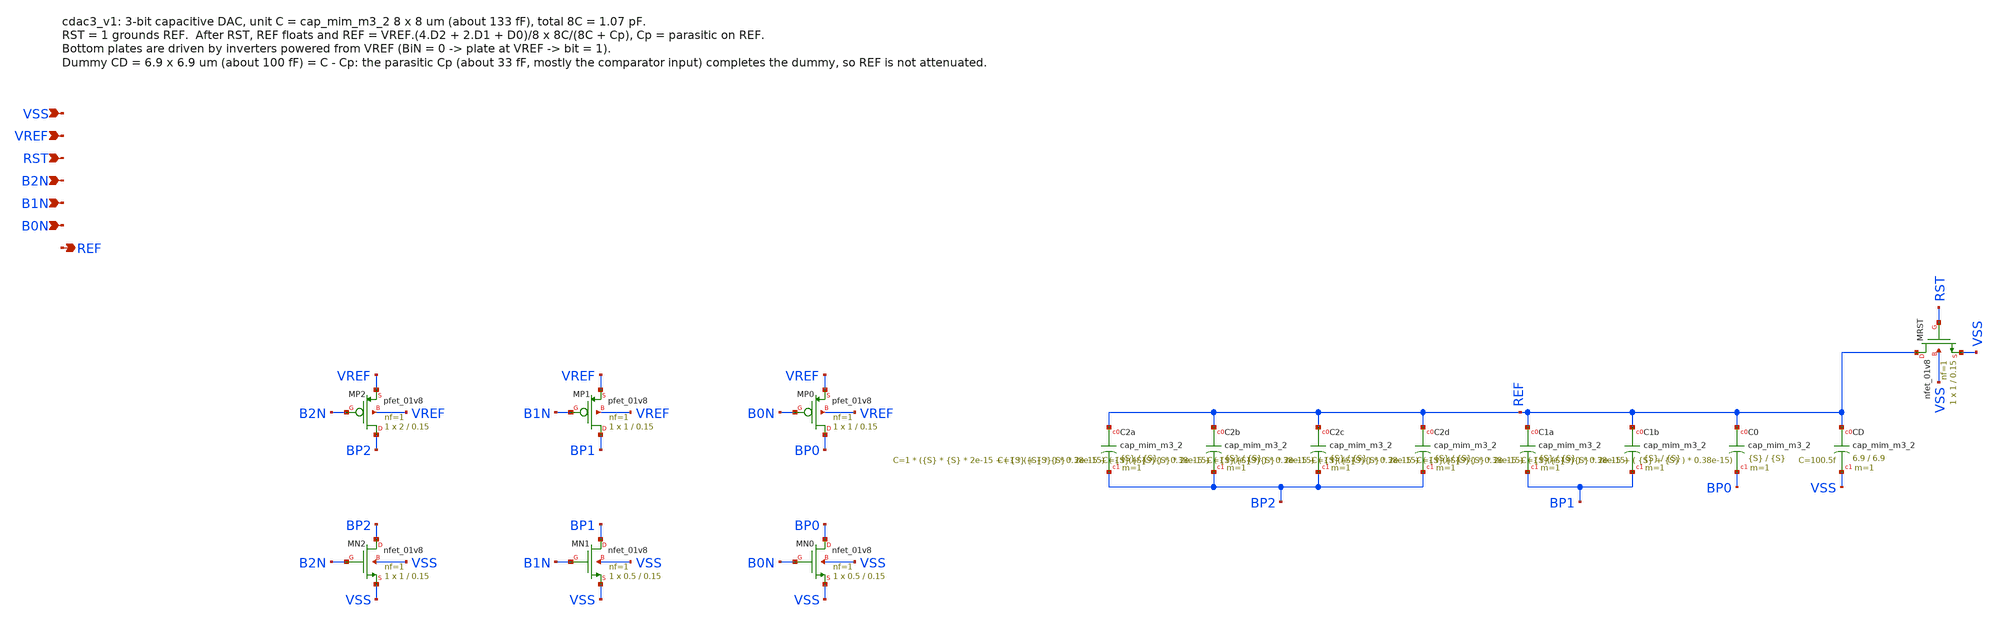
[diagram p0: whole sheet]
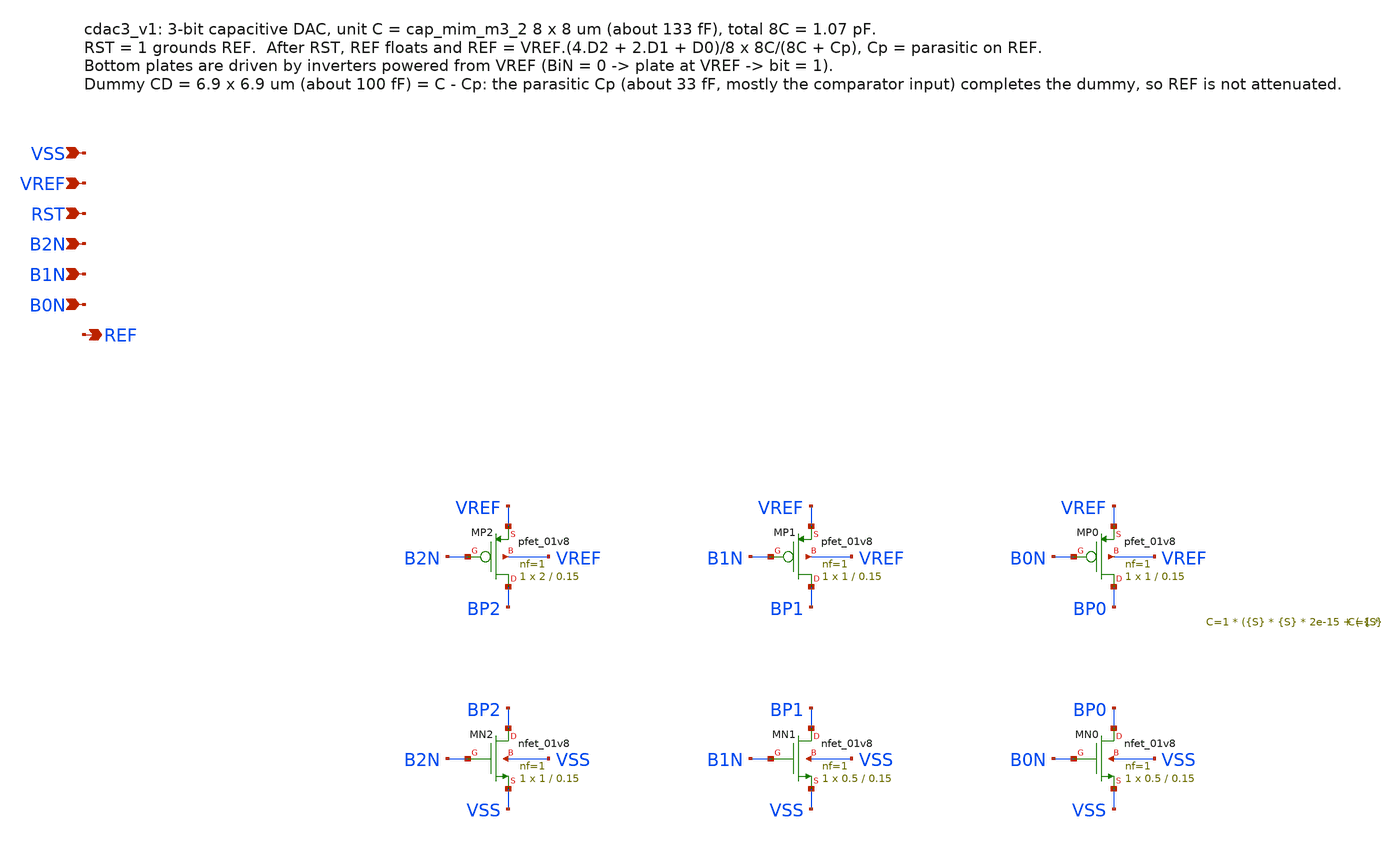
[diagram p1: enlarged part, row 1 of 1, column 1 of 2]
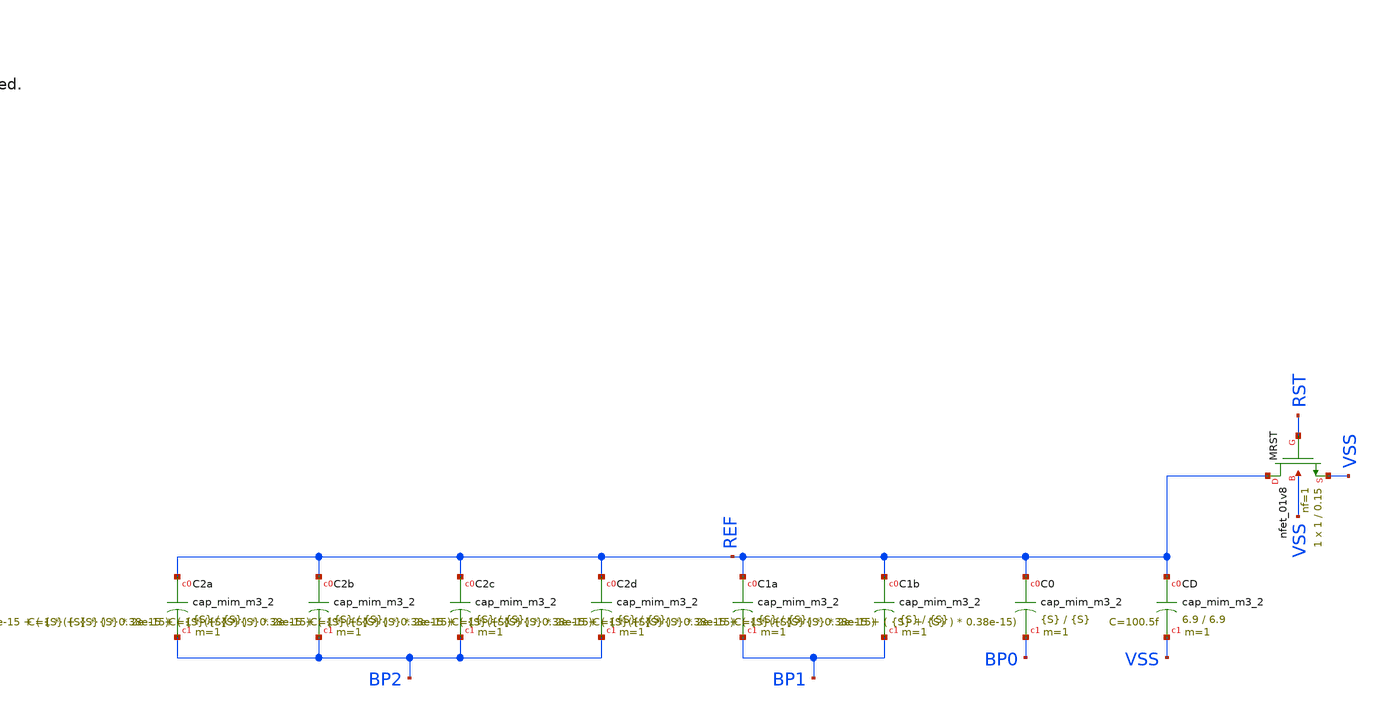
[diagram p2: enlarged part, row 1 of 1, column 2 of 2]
** sch_path: SAR_improved/cdac3_v1.sch
**.subckt cdac3_v1 VSS VREF RST B2N B1N B0N REF
*.ipin VSS
*.ipin VREF
*.ipin RST
*.ipin B2N
*.ipin B1N
*.ipin B0N
*.opin REF
XMP2 BP2 B2N VREF VREF sky130_fd_pr__pfet_01v8 L=0.15 W=2 nf=1 ad='int((nf+1)/2) * W/nf * 0.29' as='int((nf+2)/2) * W/nf * 0.29'
+ pd='2*int((nf+1)/2) * (W/nf + 0.29)' ps='2*int((nf+2)/2) * (W/nf + 0.29)' nrd='0.29 / W' nrs='0.29 / W'
+ sa=0 sb=0 sd=0 mult=1 m=1
XMN2 BP2 B2N VSS VSS sky130_fd_pr__nfet_01v8 L=0.15 W=1 nf=1 ad='int((nf+1)/2) * W/nf * 0.29' as='int((nf+2)/2) * W/nf * 0.29'
+ pd='2*int((nf+1)/2) * (W/nf + 0.29)' ps='2*int((nf+2)/2) * (W/nf + 0.29)' nrd='0.29 / W' nrs='0.29 / W'
+ sa=0 sb=0 sd=0 mult=1 m=1
XMP1 BP1 B1N VREF VREF sky130_fd_pr__pfet_01v8 L=0.15 W=1 nf=1 ad='int((nf+1)/2) * W/nf * 0.29' as='int((nf+2)/2) * W/nf * 0.29'
+ pd='2*int((nf+1)/2) * (W/nf + 0.29)' ps='2*int((nf+2)/2) * (W/nf + 0.29)' nrd='0.29 / W' nrs='0.29 / W'
+ sa=0 sb=0 sd=0 mult=1 m=1
XMN1 BP1 B1N VSS VSS sky130_fd_pr__nfet_01v8 L=0.15 W=0.5 nf=1 ad='int((nf+1)/2) * W/nf * 0.29' as='int((nf+2)/2) * W/nf * 0.29'
+ pd='2*int((nf+1)/2) * (W/nf + 0.29)' ps='2*int((nf+2)/2) * (W/nf + 0.29)' nrd='0.29 / W' nrs='0.29 / W'
+ sa=0 sb=0 sd=0 mult=1 m=1
XMP0 BP0 B0N VREF VREF sky130_fd_pr__pfet_01v8 L=0.15 W=1 nf=1 ad='int((nf+1)/2) * W/nf * 0.29' as='int((nf+2)/2) * W/nf * 0.29'
+ pd='2*int((nf+1)/2) * (W/nf + 0.29)' ps='2*int((nf+2)/2) * (W/nf + 0.29)' nrd='0.29 / W' nrs='0.29 / W'
+ sa=0 sb=0 sd=0 mult=1 m=1
XMN0 BP0 B0N VSS VSS sky130_fd_pr__nfet_01v8 L=0.15 W=0.5 nf=1 ad='int((nf+1)/2) * W/nf * 0.29' as='int((nf+2)/2) * W/nf * 0.29'
+ pd='2*int((nf+1)/2) * (W/nf + 0.29)' ps='2*int((nf+2)/2) * (W/nf + 0.29)' nrd='0.29 / W' nrs='0.29 / W'
+ sa=0 sb=0 sd=0 mult=1 m=1
XC2a REF BP2 sky130_fd_pr__cap_mim_m3_2 W={S} L={S} MF=1 m=1
XC2b REF BP2 sky130_fd_pr__cap_mim_m3_2 W={S} L={S} MF=1 m=1
XC2c REF BP2 sky130_fd_pr__cap_mim_m3_2 W={S} L={S} MF=1 m=1
XC2d REF BP2 sky130_fd_pr__cap_mim_m3_2 W={S} L={S} MF=1 m=1
XC1a REF BP1 sky130_fd_pr__cap_mim_m3_2 W={S} L={S} MF=1 m=1
XC1b REF BP1 sky130_fd_pr__cap_mim_m3_2 W={S} L={S} MF=1 m=1
XC0 REF BP0 sky130_fd_pr__cap_mim_m3_2 W={S} L={S} MF=1 m=1
XCD REF VSS sky130_fd_pr__cap_mim_m3_2 W=6.9 L=6.9 MF=1 m=1
XMRST REF RST VSS VSS sky130_fd_pr__nfet_01v8 L=0.15 W=1 nf=1 ad='int((nf+1)/2) * W/nf * 0.29' as='int((nf+2)/2) * W/nf * 0.29'
+ pd='2*int((nf+1)/2) * (W/nf + 0.29)' ps='2*int((nf+2)/2) * (W/nf + 0.29)' nrd='0.29 / W' nrs='0.29 / W'
+ sa=0 sb=0 sd=0 mult=1 m=1
**** begin user architecture code

.param S=8

**** end user architecture code
**.ends
.end
